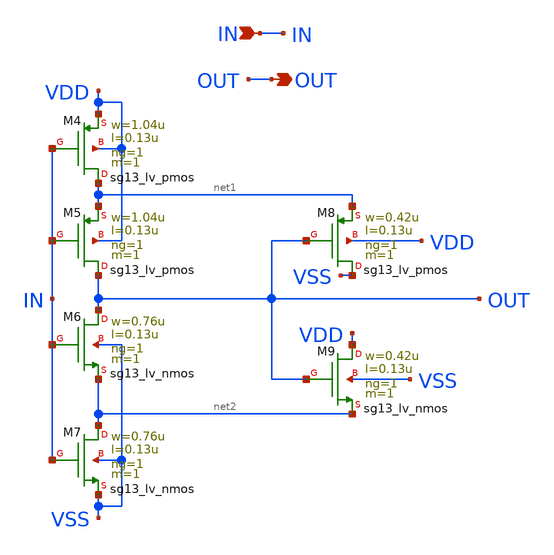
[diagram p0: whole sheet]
** sch_path: design/blocks/schmitt/schematic/schmitt.sch
**.subckt schmitt OUT IN
*.opin OUT
*.ipin IN
XM4 net1 IN VDD VDD sg13_lv_pmos w=1.04u l=0.13u ng=1 m=1 mm_ok=1
XM6 OUT IN net2 VSS sg13_lv_nmos w=0.76u l=0.13u ng=1 m=1 mm_ok=1
XM5 OUT IN net1 VDD sg13_lv_pmos w=1.04u l=0.13u ng=1 m=1 mm_ok=1
XM7 net2 IN VSS VSS sg13_lv_nmos w=0.76u l=0.13u ng=1 m=1 mm_ok=1
XM8 VSS OUT net1 VDD sg13_lv_pmos w=0.42u l=0.13u ng=1 m=1 mm_ok=1
XM9 VDD OUT net2 VSS sg13_lv_nmos w=0.42u l=0.13u ng=1 m=1 mm_ok=1
**.ends
.end
